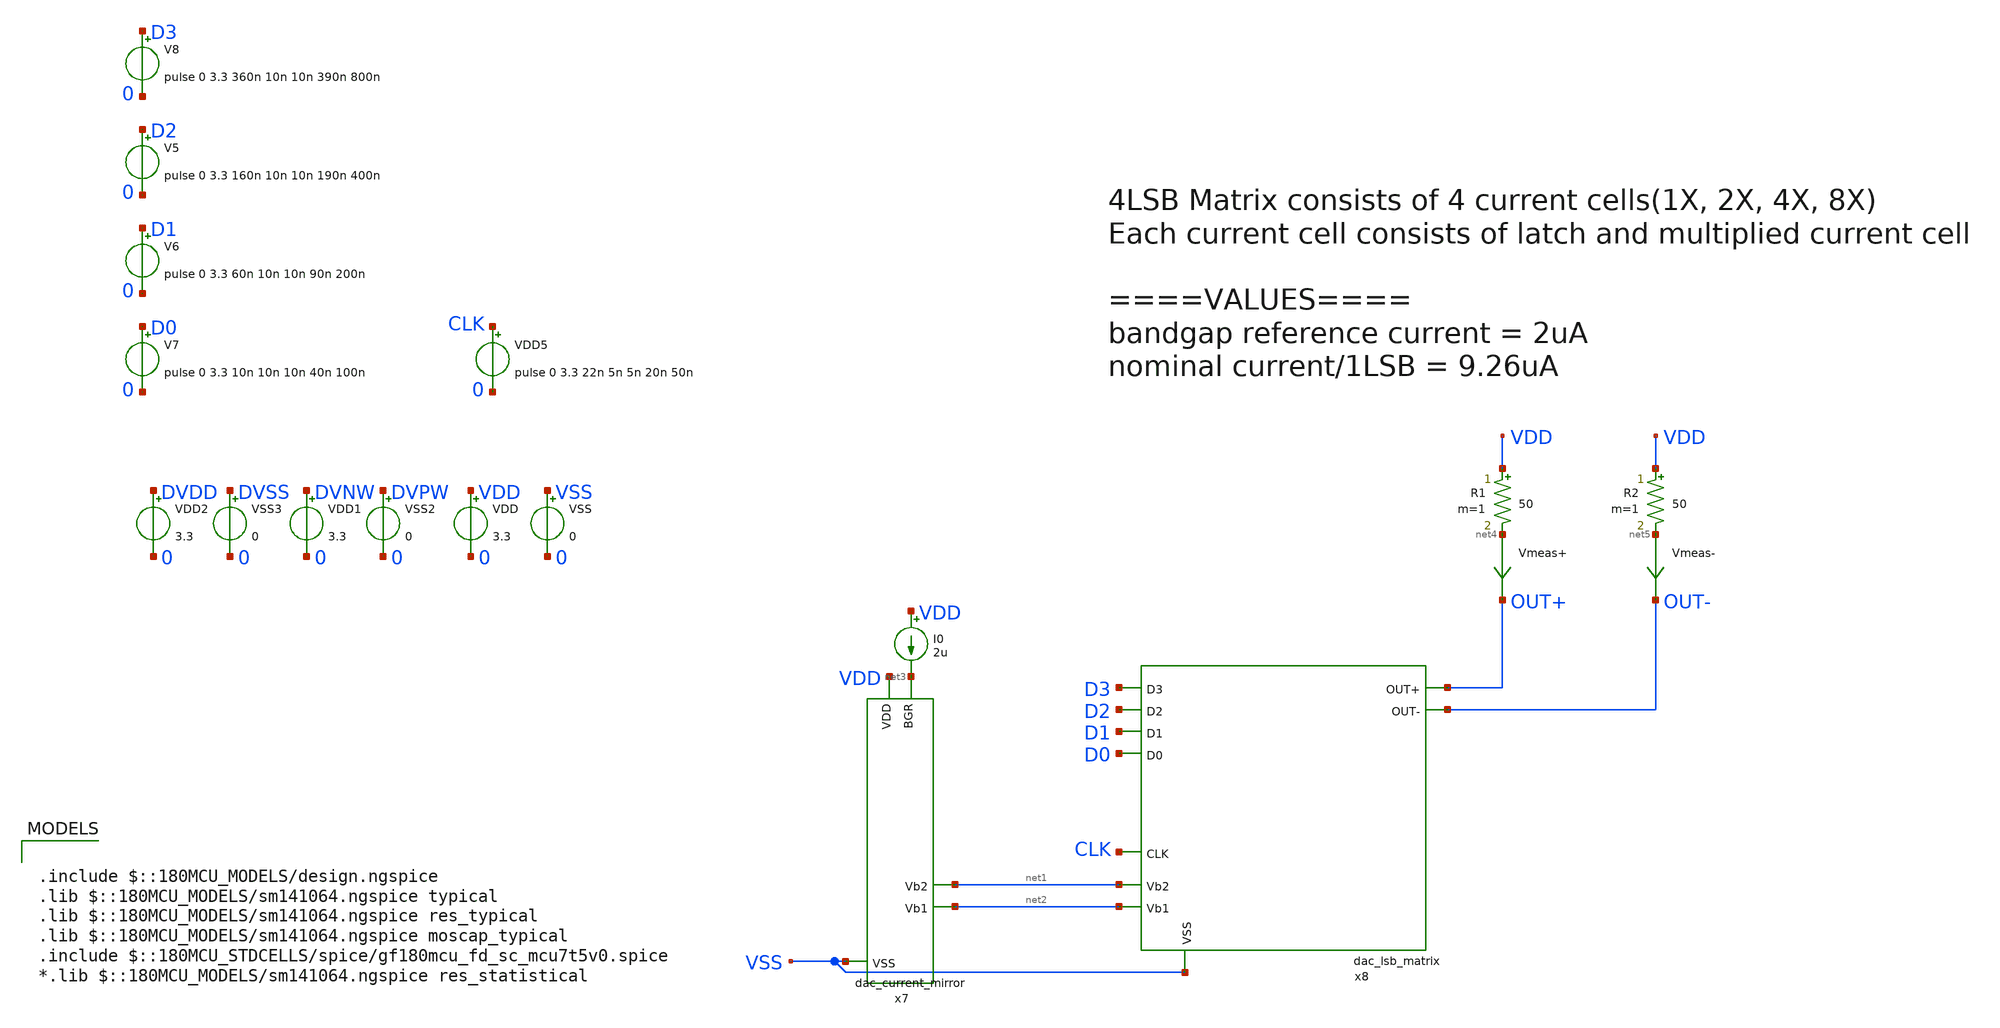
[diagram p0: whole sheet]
** sch_path: xschem/test_dac_lsb_matrix.sch
**.subckt test_dac_lsb_matrix
VDD VDD 0 3.3
VSS VSS 0 0
I0 VDD net3 2u
R1 VDD net4 50 m=1
R2 VDD net5 50 m=1
Vmeas+ net4 OUT+ 0
.save i(vmeas+)
Vmeas- net5 OUT- 0
.save i(vmeas-)
x7 VDD net3 net1 net2 VSS dac_current_mirror
VDD1 DVNW 0 3.3
VSS2 DVPW 0 0
VDD2 DVDD 0 3.3
VSS3 DVSS 0 0
x8 D2 D3 D1 D0 OUT+ OUT- CLK net1 net2 VSS DVDD DVNW DVPW DVSS dac_lsb_matrix
V5 D2 0 pulse 0 3.3 160n 10n 10n 190n 400n
V6 D1 0 pulse 0 3.3 60n 10n 10n 90n 200n
V7 D0 0 pulse 0 3.3 10n 10n 10n 40n 100n
V8 D3 0 pulse 0 3.3 360n 10n 10n 390n 800n
VDD5 CLK 0 pulse 0 3.3 22n 5n 5n 20n 50n
**** begin user architecture code


.options savecurrents
.save all
.control
	tran 1n 1000n
	plot i(Vmeas+) i(Vmeas-)
	plot v(CLK) v(D0) V(D1) V(D2) V(D3)
	write test_dac_lsb_matrix.raw
.endc



.include $::180MCU_MODELS/design.ngspice
.lib $::180MCU_MODELS/sm141064.ngspice typical
.lib $::180MCU_MODELS/sm141064.ngspice res_typical
.lib $::180MCU_MODELS/sm141064.ngspice moscap_typical
.include $::180MCU_STDCELLS/spice/gf180mcu_fd_sc_mcu7t5v0.spice
*.lib $::180MCU_MODELS/sm141064.ngspice res_statistical

**** end user architecture code
**.ends
.end
